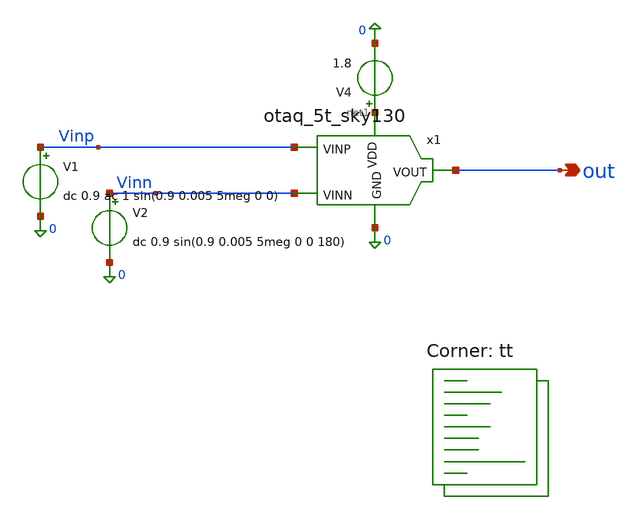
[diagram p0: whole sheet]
** sch_path: xschem/otaq_5t_sky130_tb.sch
**.subckt otaq_5t_sky130_tb out
*.opin out
V1 Vinp 0 dc 0.9 ac 1 sin(0.9 0.005 5meg 0 0)
V2 Vinn 0 dc 0.9 sin(0.9 0.005 5meg 0 0 180)
V4 net1 0 1.8
x1 net1 out Vinp Vinn 0 otaq_5t_sky130
**** begin user architecture code
.lib $::SKYWATER_MODELS/sky130.lib.spice tt


.control
save all
tran 1n 400n
write otaq5t_tran.raw
op
print @m.x1.xm2.msky130_fd_pr__nfet_01v8[gds] @m.x1.xm4.msky130_fd_pr__pfet_01v8[gds]
print @m.x1.xm1.msky130_fd_pr__nfet_01v8[gm]
write otaq5t_op.raw
ac dec 20 1k 100meg
write otaq5t_ac.raw
.endc

**** end user architecture code
**.ends

* expanding   symbol:  otaq_5t_sky130.sym # of pins=5
** sym_path: xschem/otaq_5t_sky130.sym
** sch_path: xschem/otaq_5t_sky130.sch
.subckt otaq_5t_sky130 VDD VOUT VINP VINN GND
*.ipin VINP
*.ipin VINN
*.opin VOUT
*.ipin VDD
*.ipin GND
XM5 net2 VDD GND GND sky130_fd_pr__nfet_01v8 L=20 W=0.5 nf=1 ad='int((1 + 1)/2) * 0.5 / 1 * 0.29' as='int((1 + 2)/2) * 0.5 / 1 * 0.29'
+ pd='2*int((1 + 1)/2) * (0.5 / 1 + 0.29)' ps='2*int((1 + 2)/2) * (0.5 / 1 + 0.29)' nrd='0.29 / 0.5 ' nrs='0.29 / 0.5 '
+ sa=0 sb=0 sd=0 mult=1 m=1
XM1 net1 VINP net2 GND sky130_fd_pr__nfet_01v8 L=7 W=0.5 nf=1 ad='int((1 + 1)/2) * 0.5 / 1 * 0.29' as='int((1 + 2)/2) * 0.5 / 1 * 0.29'
+ pd='2*int((1 + 1)/2) * (0.5 / 1 + 0.29)' ps='2*int((1 + 2)/2) * (0.5 / 1 + 0.29)' nrd='0.29 / 0.5 ' nrs='0.29 / 0.5 '
+ sa=0 sb=0 sd=0 mult=1 m=1
XM2 VOUT VINN net2 GND sky130_fd_pr__nfet_01v8 L=7 W=0.5 nf=1 ad='int((1 + 1)/2) * 0.5 / 1 * 0.29' as='int((1 + 2)/2) * 0.5 / 1 * 0.29'
+ pd='2*int((1 + 1)/2) * (0.5 / 1 + 0.29)' ps='2*int((1 + 2)/2) * (0.5 / 1 + 0.29)' nrd='0.29 / 0.5 ' nrs='0.29 / 0.5 '
+ sa=0 sb=0 sd=0 mult=1 m=1
XM3 net1 net1 VDD VDD sky130_fd_pr__pfet_01v8 L=7 W=1 nf=1 ad='int((1 + 1)/2) * 1 / 1 * 0.29' as='int((1 + 2)/2) * 1 / 1 * 0.29'
+ pd='2*int((1 + 1)/2) * (1 / 1 + 0.29)' ps='2*int((1 + 2)/2) * (1 / 1 + 0.29)' nrd='0.29 / 1 ' nrs='0.29 / 1 '
+ sa=0 sb=0 sd=0 mult=1 m=1
XM4 VOUT net1 VDD VDD sky130_fd_pr__pfet_01v8 L=7 W=1 nf=1 ad='int((1 + 1)/2) * 1 / 1 * 0.29' as='int((1 + 2)/2) * 1 / 1 * 0.29'
+ pd='2*int((1 + 1)/2) * (1 / 1 + 0.29)' ps='2*int((1 + 2)/2) * (1 / 1 + 0.29)' nrd='0.29 / 1 ' nrs='0.29 / 1 '
+ sa=0 sb=0 sd=0 mult=1 m=1
XM6 VDD VDD GND GND sky130_fd_pr__nfet_01v8 L=0.5 W=1 nf=1 ad='int((1 + 1)/2) * 1 / 1 * 0.29' as='int((1 + 2)/2) * 1 / 1 * 0.29'
+ pd='2*int((1 + 1)/2) * (1 / 1 + 0.29)' ps='2*int((1 + 2)/2) * (1 / 1 + 0.29)' nrd='0.29 / 1 ' nrs='0.29 / 1 '
+ sa=0 sb=0 sd=0 mult=1 m=1
.ends

.end
